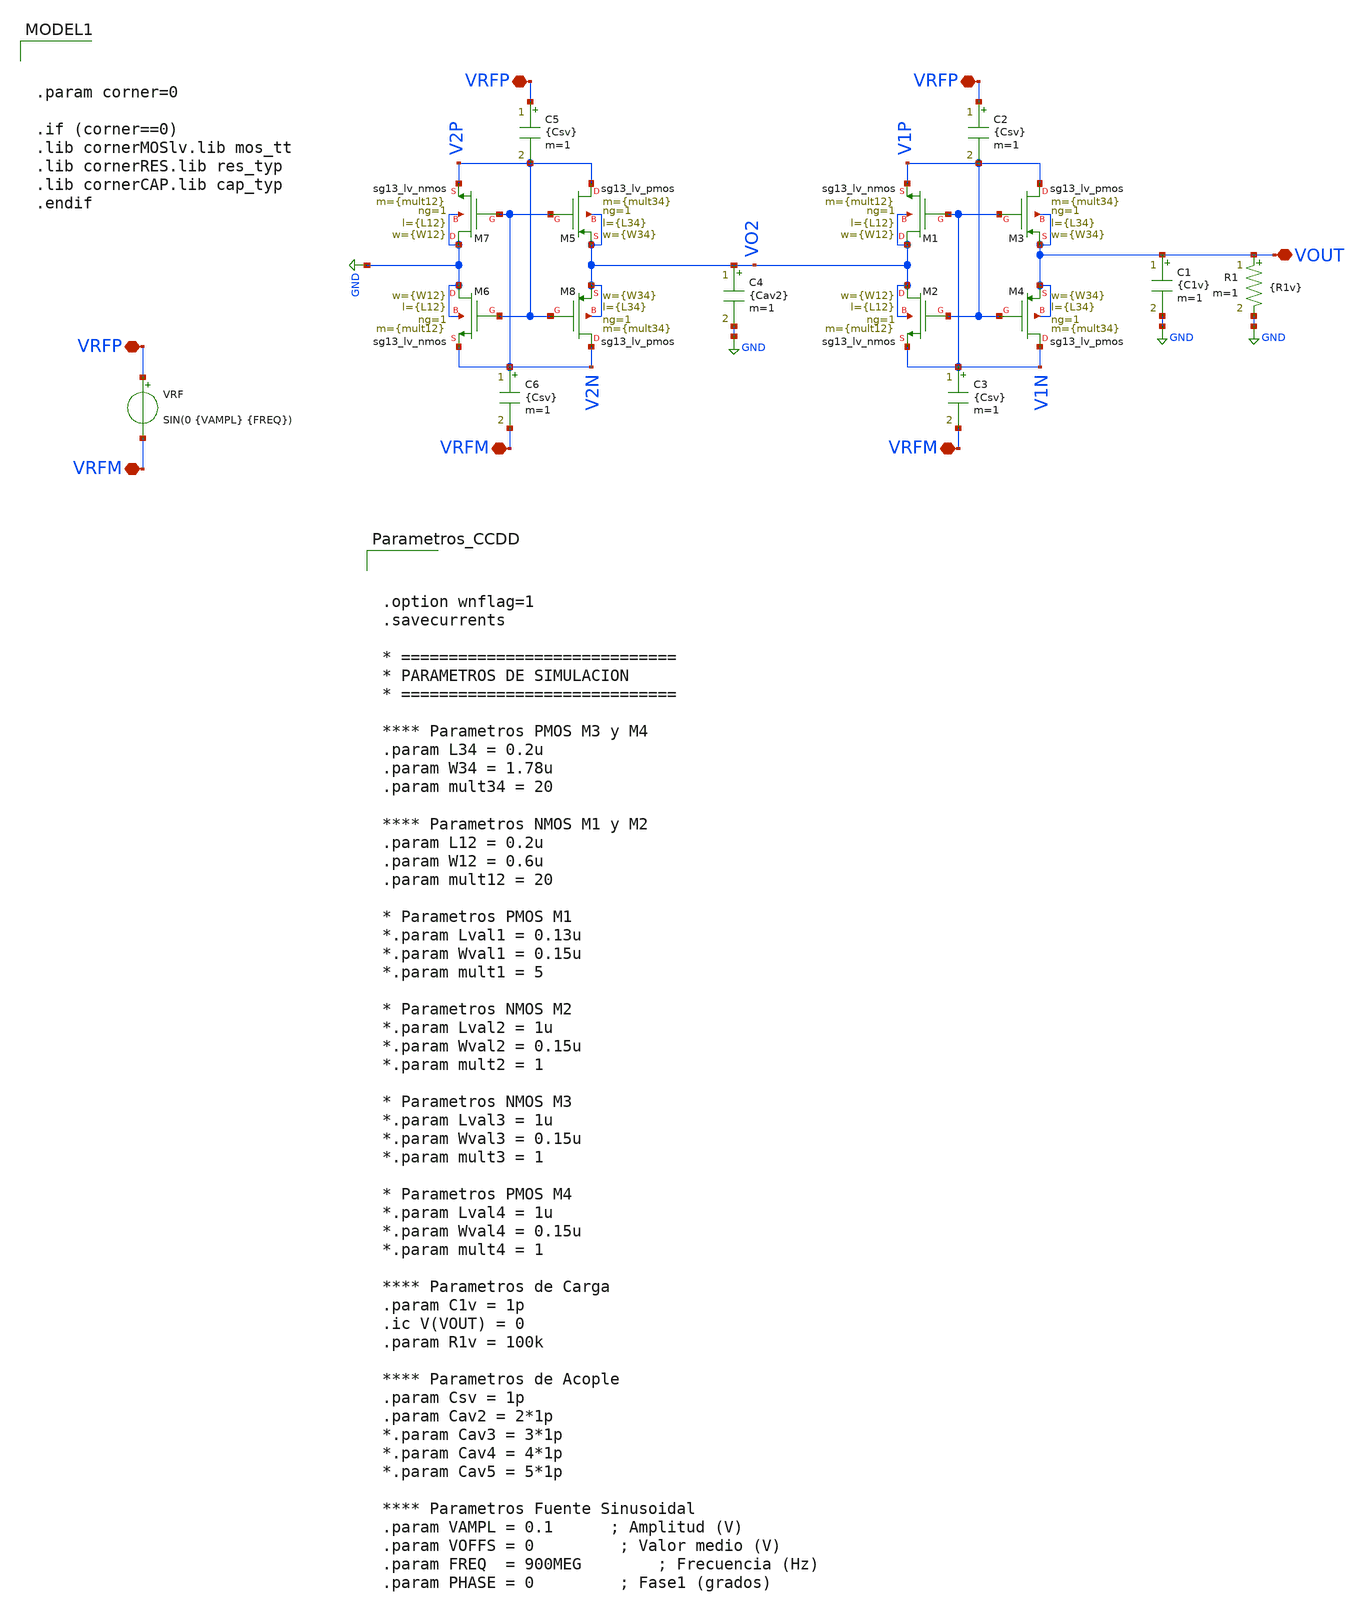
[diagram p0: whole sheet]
** sch_path: Esquematicos_Xschem/Memoria_CCDD_TRAN_MULT2.sch
**.subckt Memoria_CCDD_TRAN_MULT2 VRFP VRFM VOUT VRFP VRFM VRFP VRFM
*.iopin VRFP
*.iopin VRFM
*.iopin VOUT
*.iopin VRFP
*.iopin VRFM
*.iopin VRFP
*.iopin VRFM
XM3 V1P V1N VOUT VOUT sg13_lv_pmos w={W34} l={L34} ng=1 m={mult34} mm_ok=1
XM2 VO2 V1P V1N VO2 sg13_lv_nmos w={W12} l={L12} ng=1 m={mult12} mm_ok=1
XM1 VO2 V1N V1P VO2 sg13_lv_nmos w={W12} l={L12} ng=1 m={mult12} mm_ok=1
XM4 V1N V1P VOUT VOUT sg13_lv_pmos w={W34} l={L34} ng=1 m={mult34} mm_ok=1
R1 VOUT GND {R1v} m=1
C1 VOUT GND {C1v} m=1
VRF VRFP VRFM SIN(0 {VAMPL} {FREQ})
.save i(vrf)
C2 VRFP V1P {Csv} m=1
C3 V1N VRFM {Csv} m=1
XM5 V2P V2N VO2 VO2 sg13_lv_pmos w={W34} l={L34} ng=1 m={mult34} mm_ok=1
XM6 GND V2P V2N GND sg13_lv_nmos w={W12} l={L12} ng=1 m={mult12} mm_ok=1
XM7 GND V2N V2P GND sg13_lv_nmos w={W12} l={L12} ng=1 m={mult12} mm_ok=1
XM8 V2N V2P VO2 VO2 sg13_lv_pmos w={W34} l={L34} ng=1 m={mult34} mm_ok=1
C4 VO2 GND {Cav2} m=1
C5 VRFP V2P {Csv} m=1
C6 V2N VRFM {Csv} m=1
**** begin user architecture code



.option wnflag=1
.savecurrents

* =============================
* PARAMETROS DE SIMULACION
* =============================

**** Parametros PMOS M3 y M4
.param L34 = 0.2u
.param W34 = 1.78u
.param mult34 = 20

**** Parametros NMOS M1 y M2
.param L12 = 0.2u
.param W12 = 0.6u
.param mult12 = 20

* Parametros PMOS M1
*.param Lval1 = 0.13u
*.param Wval1 = 0.15u
*.param mult1 = 5

* Parametros NMOS M2
*.param Lval2 = 1u
*.param Wval2 = 0.15u
*.param mult2 = 1

* Parametros NMOS M3
*.param Lval3 = 1u
*.param Wval3 = 0.15u
*.param mult3 = 1

* Parametros PMOS M4
*.param Lval4 = 1u
*.param Wval4 = 0.15u
*.param mult4 = 1

**** Parametros de Carga
.param C1v = 1p
.ic V(VOUT) = 0
.param R1v = 100k

**** Parametros de Acople
.param Csv = 1p
.param Cav2 = 2*1p
*.param Cav3 = 3*1p
*.param Cav4 = 4*1p
*.param Cav5 = 5*1p

**** Parametros Fuente Sinusoidal
.param VAMPL = 0.1      ; Amplitud (V)
.param VOFFS = 0         ; Valor medio (V)
.param FREQ  = 900MEG        ; Frecuencia (Hz)
.param PHASE = 0         ; Fase1 (grados)








.option wnflag=1
.savecurrents

* ==============================================
* BLOQUE DE CONTROL NGSPICE
* ==============================================
.control

**** Compatibilidad y Color
  set filetype = ascii
  set color0 = white

**** Inicializacion de Parametro While
  let k = 0
  let start_VRF = 0.3
  let stop_VRF = 1.2
  let delta_VRF = 0.1
  let VRF_act = start_VRF

**** Inicializacion Constantes para Calculos
  let i = 0
  let IDmax = 0
  let IGmax = 0
  let VDSmax = 0
  let VGSmax = 0

**** Variables Extriores


* ==============================================
* Inicio del While
* ==============================================
  while VRF_act le stop_VRF + 2*delta_VRF
    if k = 1
      tran 20p 500n UIC
    end
    alterparam VAMPL = $&VRF_act
    reset


* -----------------------------
* Almacenamiento de Variables
* -----------------------------
    save all

    **** M2
    save @n.xm2.nsg13_lv_nmos[ids]
    save @n.xm2.nsg13_lv_nmos[igs]
    save @n.xm2.nsg13_lv_nmos[gm]
    save @n.xm2.nsg13_lv_nmos[gds]
    save @n.xm2.nsg13_lv_nmos[vth]

    **** M6
    save @n.xm6.nsg13_lv_nmos[ids]
    save @n.xm6.nsg13_lv_nmos[igs]
    save @n.xm6.nsg13_lv_nmos[gm]
    save @n.xm6.nsg13_lv_nmos[gds]
    save @n.xm6.nsg13_lv_nmos[vth]

    **** Fuente de Voltaje
    save @VRF[i]
    save @VRF[p]

    **** Carga
    save R1[i]
    save C1[i]


* ----------------------------------------------
* Definicion de Varriables Internas
* ----------------------------------------------
    if k = 1

      **** M2
      let ids2 = @n.xm2.nsg13_lv_nmos[ids]
      let igs2 = @n.xm2.nsg13_lv_nmos[igs]
      let gm2 = @n.xm2.nsg13_lv_nmos[gm]
      let gds2 =  @n.xm2.nsg13_lv_nmos[gds]
      let vth2 = @n.xm2.nsg13_lv_nmos[vth]
      let VDS2 = V1N - VO2
      let VGS2 = V1P - VO2

      **** M6
      let ids6 = @n.xm6.nsg13_lv_nmos[ids]
      let igs6 = @n.xm6.nsg13_lv_nmos[igs]
      let gm6 = @n.xm6.nsg13_lv_nmos[gm]
      let gds6 =  @n.xm6.nsg13_lv_nmos[gds]
      let vth6 = @n.xm6.nsg13_lv_nmos[vth]
      let VDS6 = V2N - 0
      let VGS6 = V2P - 0

      **** Fuente de Voltaje
      let IRF = @VRF[i]
      let PRF = @VRF[p]
      let VRF = VRFP - VRFM

      **** Carga
      let IC = @C1[i]
      let IR = @R1[i]
      let IRC = IC + IR
      let PR = IR * VOUT

    end


* ==============================================
* RESULTADOS
* ==============================================

* -----------------------------
* Graficas de la Simulacion
* -----------------------------
    if k = 1
    **** Fuente
    *plot VRF vs time
    *plot IRF vs time

    **** Carga
    plot VOUT VRF vs time
    *plot IRC vs time
    *plot avg(PR/PRF)
    end
* -----------------------------
* Registro de Datos
* -----------------------------
    remzerovec
    write Memoria_CCDD2_TRAN_MULT2_L00-20_W00-60_R100k_M20_C01-00.csv time VRF IRF VOUT VO2 IC IR
+ VDS2 VDS6 VGS2 VGS6 ids2 ids6 igs2 igs6


* ==============================================
* CIERRE DE WHILE
* ==============================================
    **** Definicion de proximo valor (while)
    let VRF_act = VRF_act + delta_VRF
    let k = 1
    set appendwrite

  end

.endc




.param corner=0

.if (corner==0)
.lib cornerMOSlv.lib mos_tt
.lib cornerRES.lib res_typ
.lib cornerCAP.lib cap_typ
.endif

**** end user architecture code
**.ends
.GLOBAL GND
.end
